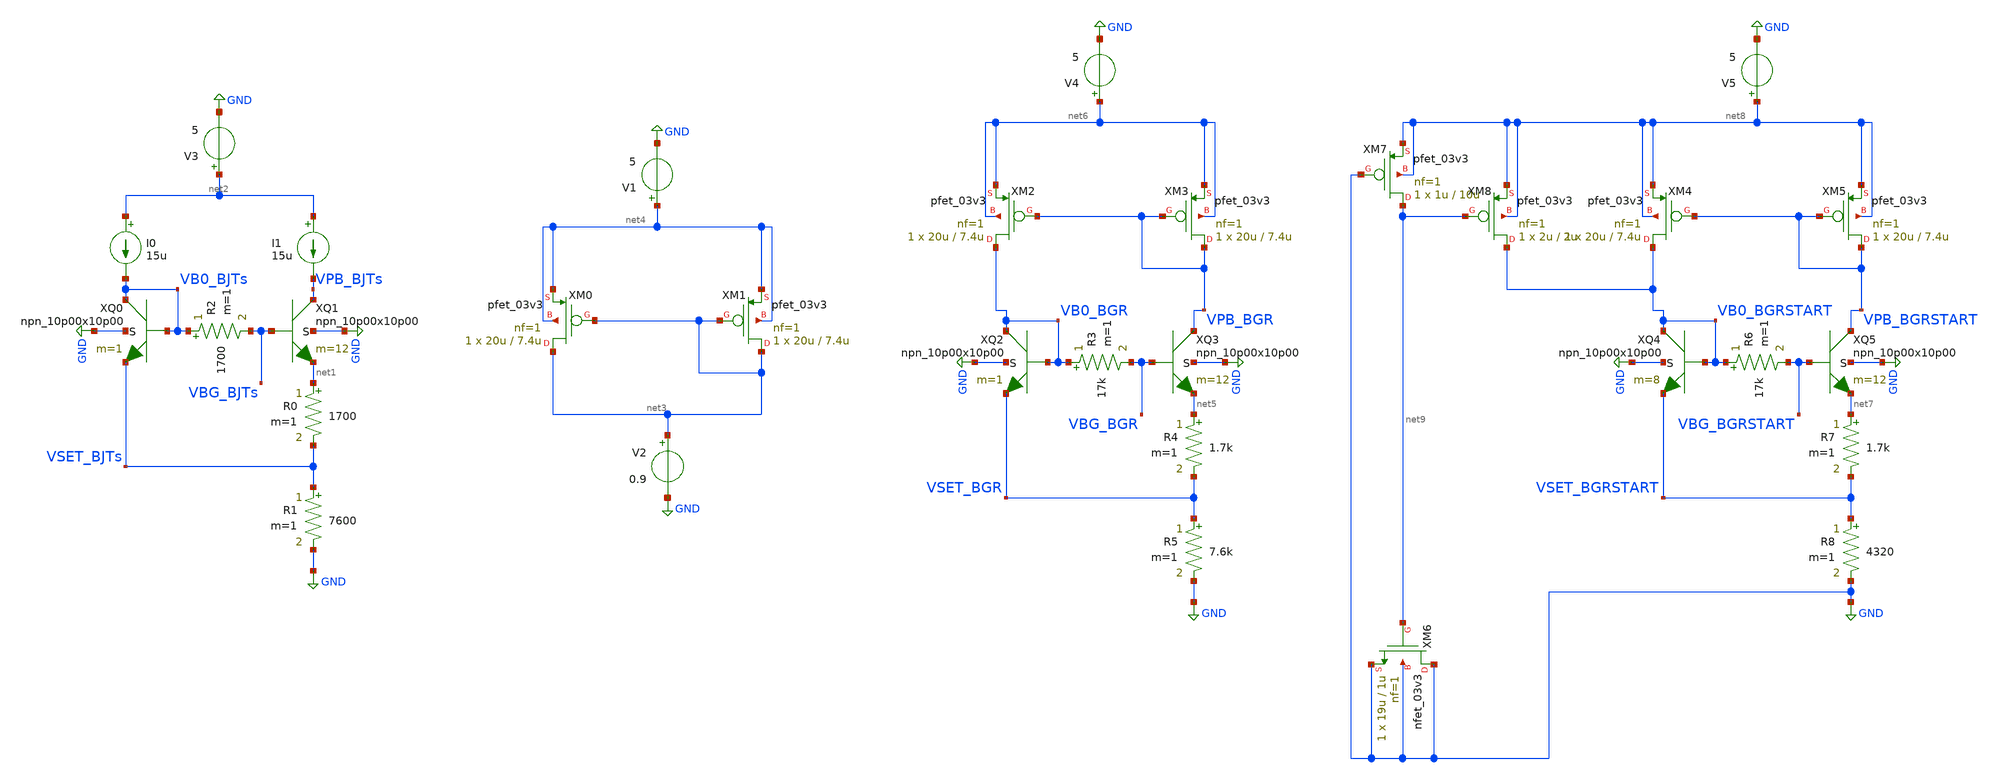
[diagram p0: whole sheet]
** sch_path: bandgap/xschem/sim/bandgap_tb_parts.sch
**.subckt bandgap_tb_parts
XQ1 VPB_BJTs VBG_BJTs net1 GND npn_10p00x10p00 m=12
XQ0 VB0_BJTs VB0_BJTs VSET_BJTs GND npn_10p00x10p00 m=1
I0 net2 VB0_BJTs 15u
I1 net2 VPB_BJTs 15u
R2 VB0_BJTs VBG_BJTs 1700 m=1
R0 net1 VSET_BJTs 1700 m=1
R1 VSET_BJTs GND 7600 m=1
XM1 net3 net3 net4 net4 pfet_03v3 L=7.4u W=20u nf=1 ad='int((nf+1)/2) * W/nf * 0.18u' as='int((nf+2)/2) * W/nf * 0.18u'
+ pd='2*int((nf+1)/2) * (W/nf + 0.18u)' ps='2*int((nf+2)/2) * (W/nf + 0.18u)' nrd='0.18u / W' nrs='0.18u / W'
+ sa=0 sb=0 sd=0 m=1
XM0 net3 net3 net4 net4 pfet_03v3 L=7.4u W=20u nf=1 ad='int((nf+1)/2) * W/nf * 0.18u' as='int((nf+2)/2) * W/nf * 0.18u'
+ pd='2*int((nf+1)/2) * (W/nf + 0.18u)' ps='2*int((nf+2)/2) * (W/nf + 0.18u)' nrd='0.18u / W' nrs='0.18u / W'
+ sa=0 sb=0 sd=0 m=1
V1 net4 GND 5
V2 net3 GND 0.9
V3 net2 GND 5
XQ3 VPB_BGR VBG_BGR net5 GND npn_10p00x10p00 m=12
XQ2 VB0_BGR VB0_BGR VSET_BGR GND npn_10p00x10p00 m=1
R3 VB0_BGR VBG_BGR 17k m=1
R4 net5 VSET_BGR 1.7k m=1
R5 VSET_BGR GND 7.6k m=1
XM3 VPB_BGR VPB_BGR net6 net6 pfet_03v3 L=7.4u W=20u nf=1 ad='int((nf+1)/2) * W/nf * 0.18u' as='int((nf+2)/2) * W/nf * 0.18u'
+ pd='2*int((nf+1)/2) * (W/nf + 0.18u)' ps='2*int((nf+2)/2) * (W/nf + 0.18u)' nrd='0.18u / W' nrs='0.18u / W'
+ sa=0 sb=0 sd=0 m=1
XM2 VB0_BGR VPB_BGR net6 net6 pfet_03v3 L=7.4u W=20u nf=1 ad='int((nf+1)/2) * W/nf * 0.18u' as='int((nf+2)/2) * W/nf * 0.18u'
+ pd='2*int((nf+1)/2) * (W/nf + 0.18u)' ps='2*int((nf+2)/2) * (W/nf + 0.18u)' nrd='0.18u / W' nrs='0.18u / W'
+ sa=0 sb=0 sd=0 m=1
V4 net6 GND 5
XQ4 VB0_BGRSTART VB0_BGRSTART VSET_BGRSTART GND npn_10p00x10p00 m=8
XQ5 VPB_BGRSTART VBG_BGRSTART net7 GND npn_10p00x10p00 m=12
R6 VB0_BGRSTART VBG_BGRSTART 17k m=1
R7 net7 VSET_BGRSTART 1.7k m=1
R8 VSET_BGRSTART GND 4320 m=1
XM4 VB0_BGRSTART VPB_BGRSTART net8 net8 pfet_03v3 L=7.4u W=20u nf=1 ad='int((nf+1)/2) * W/nf * 0.18u'
+ as='int((nf+2)/2) * W/nf * 0.18u' pd='2*int((nf+1)/2) * (W/nf + 0.18u)' ps='2*int((nf+2)/2) * (W/nf + 0.18u)'
+ nrd='0.18u / W' nrs='0.18u / W' sa=0 sb=0 sd=0 m=1
XM5 VPB_BGRSTART VPB_BGRSTART net8 net8 pfet_03v3 L=7.4u W=20u nf=1 ad='int((nf+1)/2) * W/nf * 0.18u'
+ as='int((nf+2)/2) * W/nf * 0.18u' pd='2*int((nf+1)/2) * (W/nf + 0.18u)' ps='2*int((nf+2)/2) * (W/nf + 0.18u)'
+ nrd='0.18u / W' nrs='0.18u / W' sa=0 sb=0 sd=0 m=1
V5 net8 GND 5
XM6 GND net9 GND GND nfet_03v3 L=1u W=19u nf=1 ad='int((nf+1)/2) * W/nf * 0.18u' as='int((nf+2)/2) * W/nf * 0.18u'
+ pd='2*int((nf+1)/2) * (W/nf + 0.18u)' ps='2*int((nf+2)/2) * (W/nf + 0.18u)' nrd='0.18u / W' nrs='0.18u / W'
+ sa=0 sb=0 sd=0 m=1
XM7 net9 GND net8 net8 pfet_03v3 L=10u W=1u nf=1 ad='int((nf+1)/2) * W/nf * 0.18u' as='int((nf+2)/2) * W/nf * 0.18u'
+ pd='2*int((nf+1)/2) * (W/nf + 0.18u)' ps='2*int((nf+2)/2) * (W/nf + 0.18u)' nrd='0.18u / W' nrs='0.18u / W'
+ sa=0 sb=0 sd=0 m=1
XM8 VB0_BGRSTART net9 net8 net8 pfet_03v3 L=2u W=2u nf=1 ad='int((nf+1)/2) * W/nf * 0.18u' as='int((nf+2)/2) * W/nf * 0.18u'
+ pd='2*int((nf+1)/2) * (W/nf + 0.18u)' ps='2*int((nf+2)/2) * (W/nf + 0.18u)' nrd='0.18u / W' nrs='0.18u / W'
+ sa=0 sb=0 sd=0 m=1
**** begin user architecture code


.temp 27
.option method=gear
.param L_VAR = 7.4u
.control
save all

op
echo BJTs
print @q.xq0.q0[vbe]
print @q.xq1.q0[vbe]
print @q.xq0.q0[ie]
print @q.xq1.q0[ie]
print v(VB0_BJTs)
print v(VPB_BJTs)
print v(VSET_BJTs)
print v(VBG_BJTs)

echo Mirrors
print @m.xm0.m0[id]
print @m.xm1.m0[id]

echo BGR
print @q.xq2.q0[vbe]
print @q.xq3.q0[vbe]
print @q.xq2.q0[ie]
print @q.xq3.q0[ie]
print @m.xm2.m0[id]
print @m.xm3.m0[id]
print v(VB0_BGR)
print v(VPB_BGR)
print v(VSET_BGR)
print v(VBG_BGR)

echo BGRSTART
print @q.xq4.q0[vbe]
print @q.xq5.q0[vbe]
print @q.xq4.q0[ie]
print @q.xq5.q0[ie]
print @m.xm4.m0[id]
print @m.xm5.m0[id]
print v(VB0_BGRSTART)
print v(VPB_BGRSTART)
print v(VSET_BGRSTART)
print v(VBG_BGRSTART)


*.param L_VAR = 7u
*echo Corrent_L_7u
*print @m.xm0.m0[id]
*alterparam L_VAR = 8u
*reset
*op
*echo Corrent_L_8u
*print @m.xm0.m0[id]

write bandgap_tb_parts.raw
.endc



.include $::180MCU_MODELS/design.ngspice

.lib $::180MCU_MODELS/sm141064.ngspice typical
.lib $::180MCU_MODELS/sm141064.ngspice res_typical
.lib $::180MCU_MODELS/sm141064.ngspice moscap_typical
.lib $::180MCU_MODELS/sm141064.ngspice bjt_typical
.lib $::180MCU_MODELS/sm141064.ngspice cap_mim
.lib $::180MCU_MODELS/sm141064.ngspice mimcap_typical

**** end user architecture code
**.ends
.GLOBAL GND
.end
